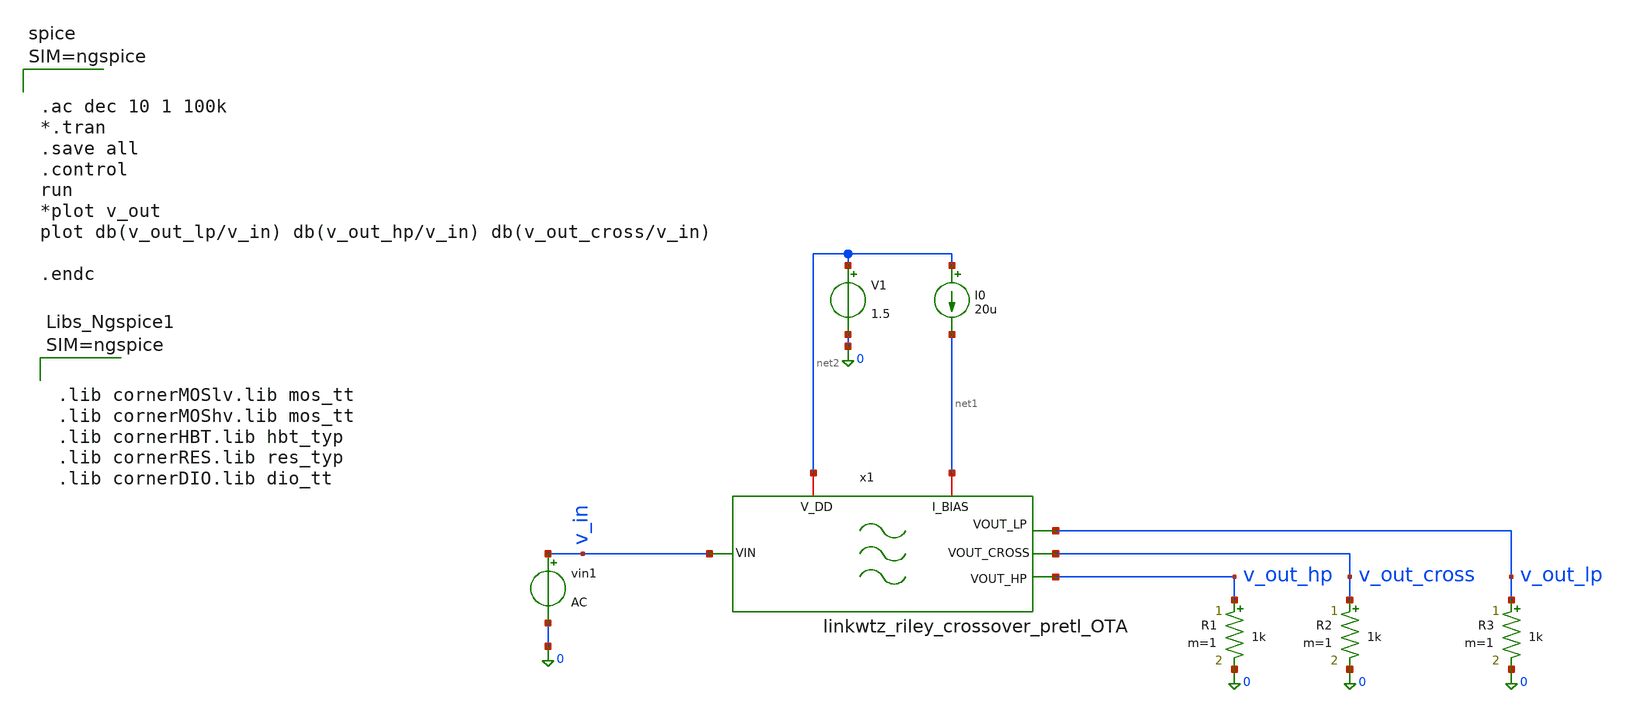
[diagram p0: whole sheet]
** sch_path: 004_Real_Circuits/linkwitz_riley_real_circuit_pretl_top_tb.sch
* 004_Real_Circuits/ota-5t.sch:
* (c) 2024-2025 Harald Pretl, Apache-2.0 license
**.subckt linkwitz_riley_real_circuit_pretl_top_tb
I0 net2 net1 20u
V1 net2 0 1.5
vin1 v_in 0 AC
R2 v_out_cross 0 1k m=1
R3 v_out_lp 0 1k m=1
R1 v_out_hp 0 1k m=1
x1 net2 net1 v_out_lp v_out_cross v_in v_out_hp linkwtz_riley_crossover_pretl_OTA
**** begin user architecture code



.lib cornerMOSlv.lib mos_tt
.lib cornerMOShv.lib mos_tt
.lib cornerHBT.lib hbt_typ
.lib cornerRES.lib res_typ
.lib cornerDIO.lib dio_tt






.ac dec 10 1 100k
*.tran
.save all
.control
run
*plot v_out
plot db(v_out_lp/v_in) db(v_out_hp/v_in) db(v_out_cross/v_in)

.endc



**** end user architecture code
**.ends

* expanding   symbol:
*+  /foss/designs/GitHub_Repo/004_Real_Circuits/linkwtz_riley_crossover_pretl_OTA.sym # of pins=6
** sym_path: 004_Real_Circuits/linkwtz_riley_crossover_pretl_OTA.sym
** sch_path: 004_Real_Circuits/linkwtz_riley_crossover_pretl_OTA.sch
.subckt linkwtz_riley_crossover_pretl_OTA V_DD I_BIAS VOUT_LP VOUT_CROSS VIN VOUT_HP
*.opin VOUT_LP
*.opin VOUT_HP
*.ipin VIN
*.iopin I_BIAS
*.iopin V_DD
*.opin VOUT_CROSS
R1 net1 VIN R_LP m=1
.param C_LP=1.06e-6
.param R_LP=1000
.param C_HP=1e-9
.param R_HP=1.06e6
.param R_IN=1k
R2 net2 net1 R_LP m=1
C1 net2 0 C_LP m=1
C2 net1 VOUT_LP C_LP m=1
C3 VIN net3 C_HP m=1
C4 net3 net4 C_HP m=1
R3 net3 VOUT_HP R_HP m=1
R4 net4 0 R_HP m=1
R10 net5 net6 R_IN m=1
R11 VOUT_HP net5 R_IN m=1
R12 net7 VOUT_CROSS R_IN m=1
R13 net6 net7 R_IN m=1
R14 VOUT_LP net7 R_IN m=1
E1 net6 0 0 net5 1e6
E4 VOUT_CROSS 0 0 net7 1e6
x1 V_DD VOUT_LP net2 VOUT_LP I_BIAS V_DD 0 ota-5t
x2 V_DD VOUT_HP net4 VOUT_HP I_BIAS V_DD 0 ota-5t
.ends


* expanding   symbol:  /foss/designs/GitHub_Repo/004_Real_Circuits/ota-5t.sym # of pins=7
** sym_path: /foss/designs/GitHub_Repo/004_Real_Circuits/ota-5t.sym
** sch_path: /foss/designs/GitHub_Repo/004_Real_Circuits/ota-5t.sch
.subckt ota-5t vdd vout vinp vinn ibias_20u d_ena vss
*.ipin ibias_20u
*.iopin vdd
*.iopin vss
*.ipin vinp
*.ipin vinn
*.opin vout
*.ipin d_ena
XM5 tail gate_n vss vss sg13_lv_nmos w=1.0u l=5u ng=1 m=1 mm_ok=1
XM4 vout gate_p vdd vdd sg13_lv_pmos w=2.5u l=5u ng=1 m=1 mm_ok=1
XM1 gate_p vinp tail vss sg13_lv_nmos w=2u l=5u ng=1 m=1 mm_ok=1
XM2 vout vinn tail vss sg13_lv_nmos w=2u l=5u ng=1 m=1 mm_ok=1
XM3 gate_p gate_p vdd vdd sg13_lv_pmos w=2.5u l=5u ng=1 m=1 mm_ok=1
XM6 ibias_20u gate_n vss vss sg13_lv_nmos w=6.5u l=5u ng=5 m=1 mm_ok=1
XM9 gate_n ena_n vss vss sg13_lv_nmos w=0.5u l=0.13u ng=1 m=1 mm_ok=1
XM11 gate_p ena vdd vdd sg13_lv_pmos w=1.5u l=0.13u ng=1 m=1 mm_ok=1
XM7 ena ena_n vss vss sg13_lv_nmos w=0.5u l=0.13u ng=1 m=1 mm_ok=1
XM8 ena ena_n vdd vdd sg13_lv_pmos w=1.5u l=0.13u ng=1 m=1 mm_ok=1
XM10 ibias_20u ena gate_n vss sg13_lv_nmos w=0.5u l=0.13u ng=1 m=1 mm_ok=1
XM12 ena_n d_ena vss vss sg13_lv_nmos w=0.5u l=0.13u ng=1 m=1 mm_ok=1
XM13 ena_n d_ena vdd vdd sg13_lv_pmos w=1.5u l=0.13u ng=1 m=1 mm_ok=1
.ends

.end
